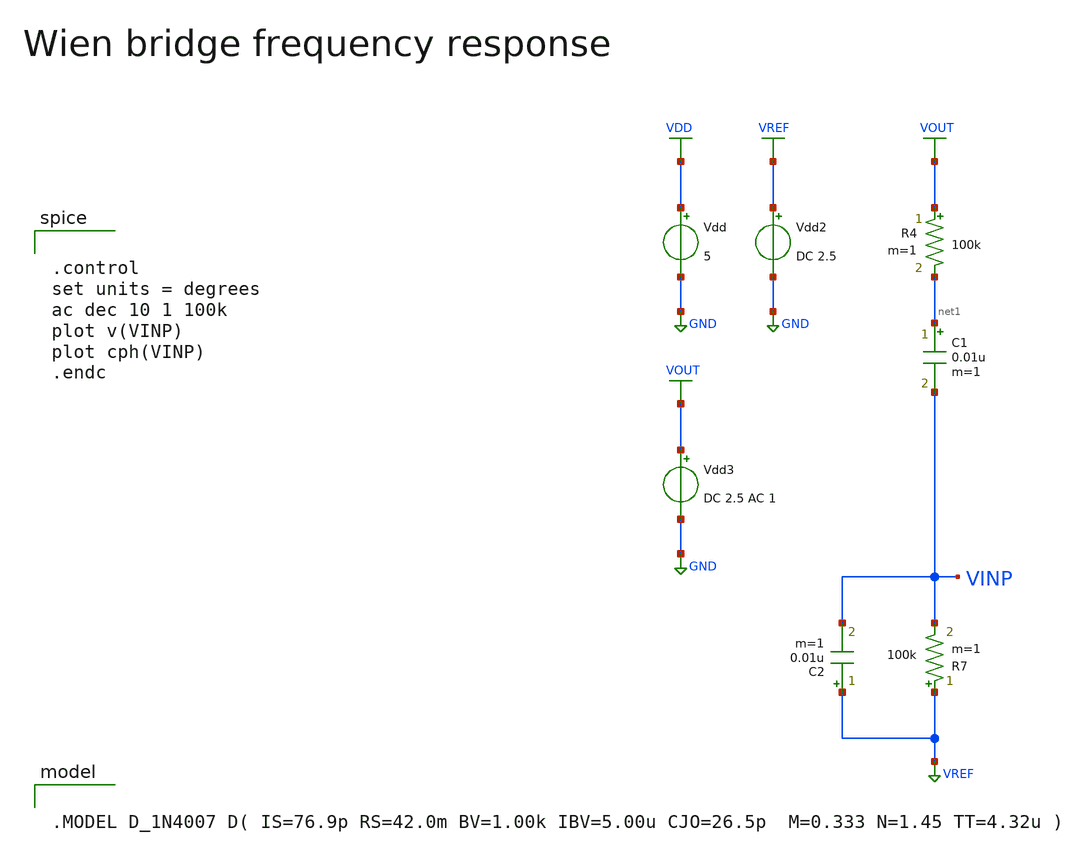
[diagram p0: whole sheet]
** sch_path: Vol.2/files/08/xschem/tb_wien_bridge_freq_res.sch
**.subckt tb_wien_bridge_freq_res
Vdd VDD GND 5
Vdd2 VREF GND DC 2.5
R4 VOUT net1 100k m=1
C1 net1 VINP 0.01u m=1
R7 VREF VINP 100k m=1
C2 VREF VINP 0.01u m=1
Vdd3 VOUT GND DC 2.5 AC 1
**** begin user architecture code


.control
set units = degrees
ac dec 10 1 100k
plot v(VINP)
plot cph(VINP)
.endc




.MODEL D_1N4007 D( IS=76.9p RS=42.0m BV=1.00k IBV=5.00u CJO=26.5p  M=0.333 N=1.45 TT=4.32u )


**** end user architecture code
**.ends
.GLOBAL VDD
.GLOBAL GND
.GLOBAL VREF
.GLOBAL VOUT
.end
